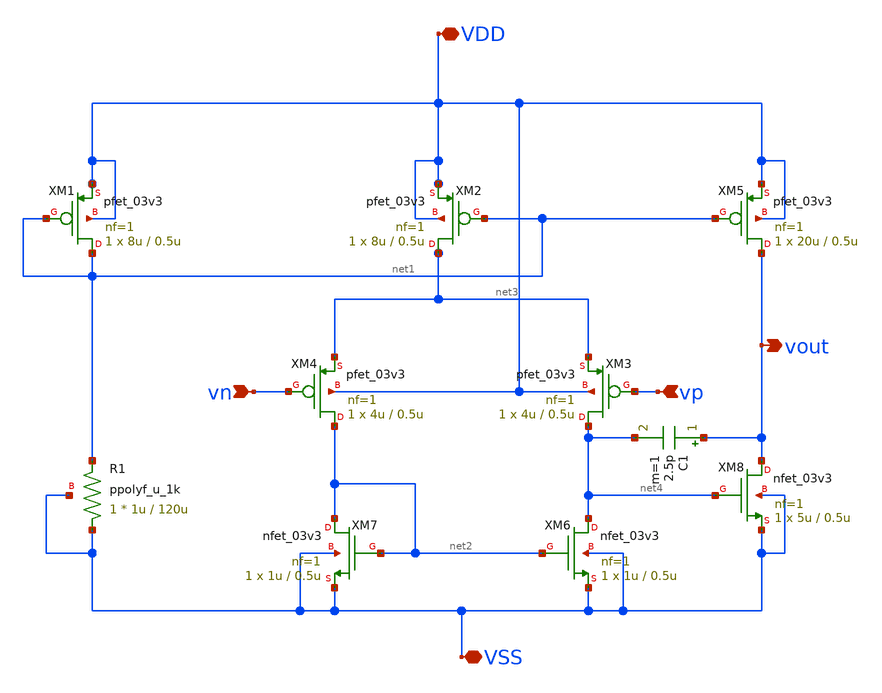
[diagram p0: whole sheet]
** sch_path: xschem/amp.sch
**.subckt amp VDD VSS vn vp vout
*.iopin VDD
*.iopin VSS
*.ipin vn
*.ipin vp
*.opin vout
XM1 net1 net1 VDD VDD pfet_03v3 L=0.5u W=8u nf=1 ad='int((nf+1)/2) * W/nf * 0.18u' as='int((nf+2)/2) * W/nf * 0.18u'
+ pd='2*int((nf+1)/2) * (W/nf + 0.18u)' ps='2*int((nf+2)/2) * (W/nf + 0.18u)' nrd='0.18u / W' nrs='0.18u / W'
+ sa=0 sb=0 sd=0 m=1 par=1
XM2 net3 net1 VDD VDD pfet_03v3 L=0.5u W=8u nf=1 ad='int((nf+1)/2) * W/nf * 0.18u' as='int((nf+2)/2) * W/nf * 0.18u'
+ pd='2*int((nf+1)/2) * (W/nf + 0.18u)' ps='2*int((nf+2)/2) * (W/nf + 0.18u)' nrd='0.18u / W' nrs='0.18u / W'
+ sa=0 sb=0 sd=0 m=1 par=1
XM3 net4 vp net3 VDD pfet_03v3 L=0.5u W=4u nf=1 ad='int((nf+1)/2) * W/nf * 0.18u' as='int((nf+2)/2) * W/nf * 0.18u'
+ pd='2*int((nf+1)/2) * (W/nf + 0.18u)' ps='2*int((nf+2)/2) * (W/nf + 0.18u)' nrd='0.18u / W' nrs='0.18u / W'
+ sa=0 sb=0 sd=0 m=1 par=1
XM4 net2 vn net3 VDD pfet_03v3 L=0.5u W=4u nf=1 ad='int((nf+1)/2) * W/nf * 0.18u' as='int((nf+2)/2) * W/nf * 0.18u'
+ pd='2*int((nf+1)/2) * (W/nf + 0.18u)' ps='2*int((nf+2)/2) * (W/nf + 0.18u)' nrd='0.18u / W' nrs='0.18u / W'
+ sa=0 sb=0 sd=0 m=1 par=1
XM5 vout net1 VDD VDD pfet_03v3 L=0.5u W=20u nf=1 ad='int((nf+1)/2) * W/nf * 0.18u' as='int((nf+2)/2) * W/nf * 0.18u'
+ pd='2*int((nf+1)/2) * (W/nf + 0.18u)' ps='2*int((nf+2)/2) * (W/nf + 0.18u)' nrd='0.18u / W' nrs='0.18u / W'
+ sa=0 sb=0 sd=0 m=1 par=1
XM6 net4 net2 VSS VSS nfet_03v3 L=0.5u W=1u nf=1 ad='int((nf+1)/2) * W/nf * 0.18u' as='int((nf+2)/2) * W/nf * 0.18u'
+ pd='2*int((nf+1)/2) * (W/nf + 0.18u)' ps='2*int((nf+2)/2) * (W/nf + 0.18u)' nrd='0.18u / W' nrs='0.18u / W'
+ sa=0 sb=0 sd=0 m=1 par=1
XM8 vout net4 VSS VSS nfet_03v3 L=0.5u W=5u nf=1 ad='int((nf+1)/2) * W/nf * 0.18u' as='int((nf+2)/2) * W/nf * 0.18u'
+ pd='2*int((nf+1)/2) * (W/nf + 0.18u)' ps='2*int((nf+2)/2) * (W/nf + 0.18u)' nrd='0.18u / W' nrs='0.18u / W'
+ sa=0 sb=0 sd=0 m=1 par=1
XR1 VSS net1 VSS ppolyf_u_1k r_width=1u r_length=120u m=1
C1 vout net4 2.5p m=1
XM7 net2 net2 VSS VSS nfet_03v3 L=0.5u W=1u nf=1 ad='int((nf+1)/2) * W/nf * 0.18u' as='int((nf+2)/2) * W/nf * 0.18u'
+ pd='2*int((nf+1)/2) * (W/nf + 0.18u)' ps='2*int((nf+2)/2) * (W/nf + 0.18u)' nrd='0.18u / W' nrs='0.18u / W'
+ sa=0 sb=0 sd=0 m=1 par=1
**.ends
.end
